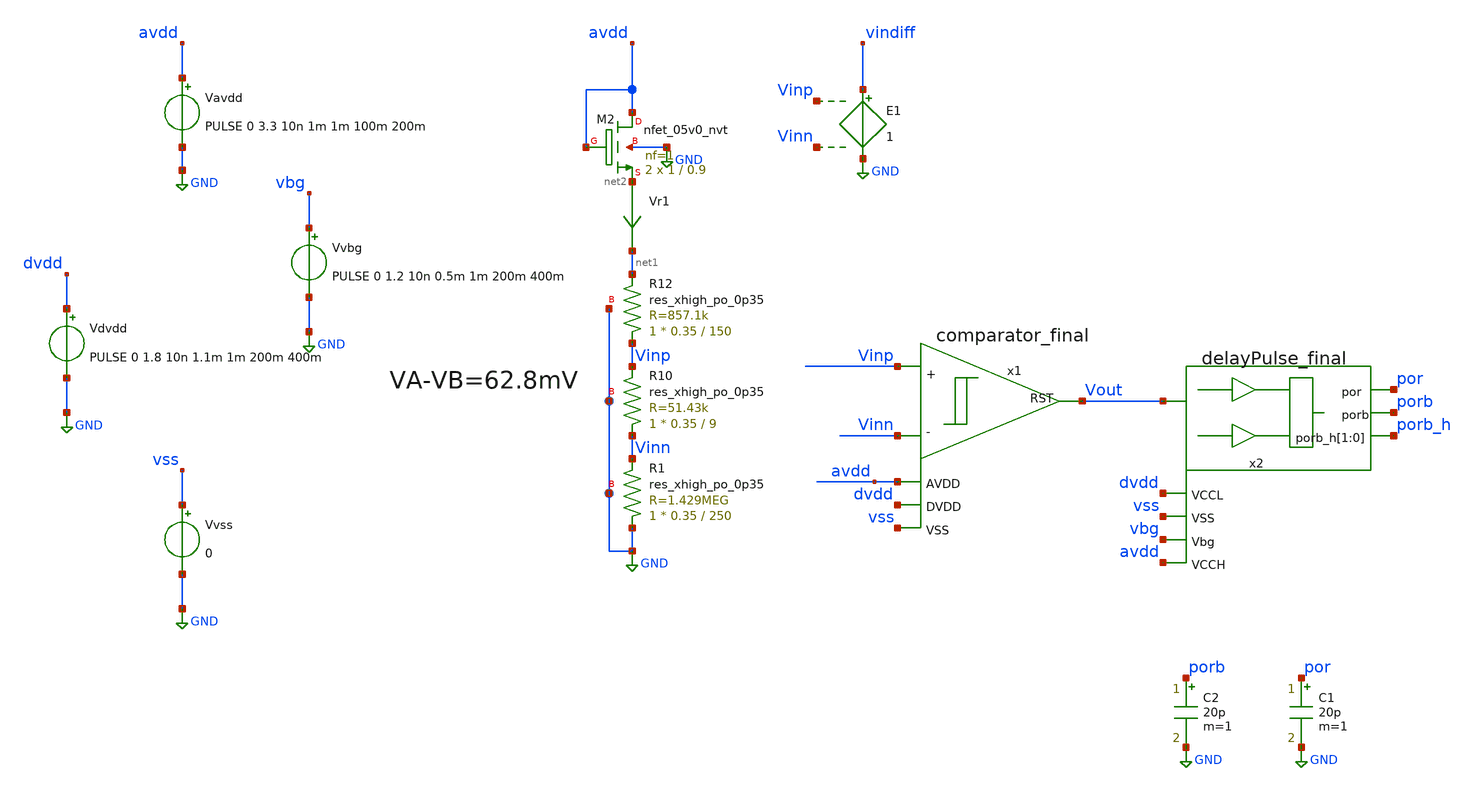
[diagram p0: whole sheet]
** sch_path: xschem/top_por_final.sch
**.subckt top_por_final
Vr1 net2 net1 0
.save i(vr1)
E1 vindiff GND Vinp Vinn 1
x1 Vinn Vinp Vout vss avdd dvdd comparator_final
XR1 GND Vinn GND sky130_fd_pr__res_xhigh_po_0p35 L=250 mult=1 m=1
XR10 Vinn Vinp GND sky130_fd_pr__res_xhigh_po_0p35 L=9 mult=1 m=1
XR12 Vinp net1 GND sky130_fd_pr__res_xhigh_po_0p35 L=150 mult=1 m=1
x2 Vout por dvdd vss vbg avdd porb porb_h porb_h delayPulse_final
XM2 avdd avdd net2 GND sky130_fd_pr__nfet_05v0_nvt L=0.9 W=1 nf=1 ad='int((nf+1)/2) * W/nf * 0.29' as='int((nf+2)/2) * W/nf * 0.29'
+ pd='2*int((nf+1)/2) * (W/nf + 0.29)' ps='2*int((nf+2)/2) * (W/nf + 0.29)' nrd='0.29 / W' nrs='0.29 / W'
+ sa=0 sb=0 sd=0 mult=2 m=2
Vdvdd dvdd GND PULSE 0 1.8 10n 1.1m 1m 200m 400m
Vvbg vbg GND PULSE 0 1.2 10n 0.5m 1m 200m 400m
Vvss vss GND 0
Vavdd avdd GND PULSE 0 3.3 10n 1m 1m 100m 200m
C1 por GND 20p m=1
C2 porb GND 20p m=1
**** begin user architecture code
 .lib $::SKYWATER_MODELS/sky130.lib.spice tt

.include $::SKYWATER_STDCELLS/sky130_fd_sc_hd.spice
.include $::SKYWATER_STDCELLS/../../sky130_fd_sc_hvl/spice/sky130_fd_sc_hvl.spice





* ngspice commands

.options savecurrents

.control
  set temp=27
  save all
  save @m.xm1.msky130_fd_pr__nfet_05v0_nvt[gm]
  save @m.xm1.msky130_fd_pr__nfet_05v0_nvt[id]
  op
  write top_por_final.raw
  set appendwrite
  tran 1u 55m
  *tran 1u 2m
  *tran 1u 100m
  meas tran Ivdd AVG i(Vavdd)
  meas tran yAvdd FIND v(avdd) WHEN v(por)=0.9 RISE=1
  meas tran porPulse TRIG v(por) VAL=0.9 RISE=1 TARG v(por) VAL=0.9 FALL=1
  write top_por_final.raw
  *quit 0

.endc



**** end user architecture code
**.ends
.GLOBAL GND
.end
